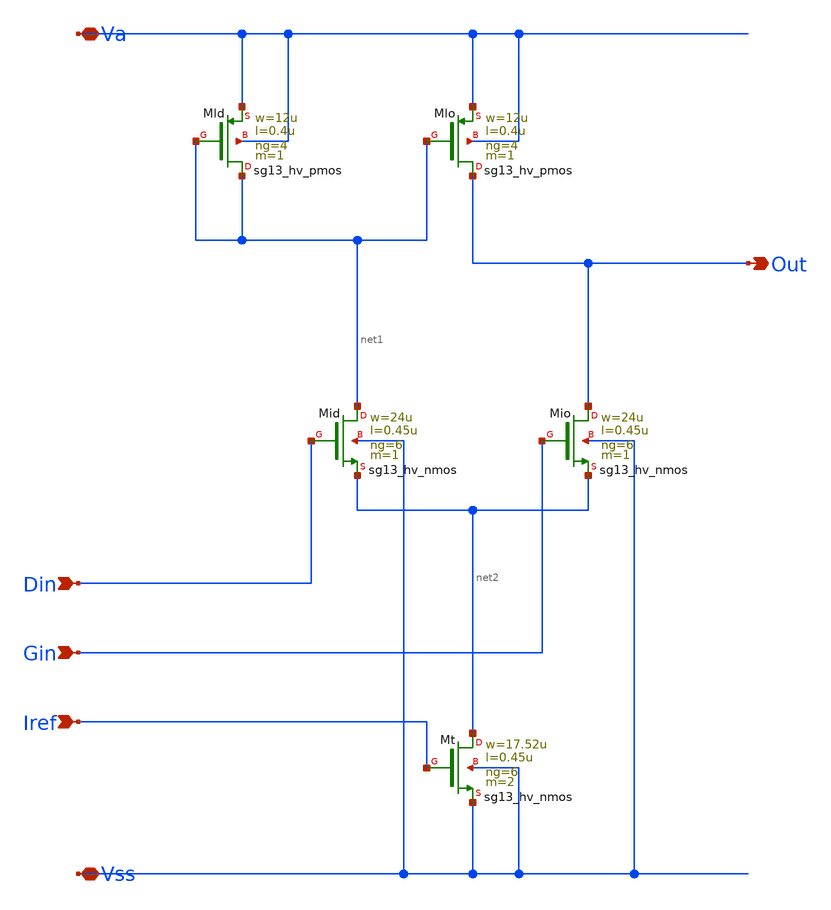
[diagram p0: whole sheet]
** sch_path: macros/lvds_tx/schematic/xschem/predriver_comp.sch
**.subckt predriver_comp Va Vss Out Din Gin Iref
*.iopin Va
*.iopin Vss
*.opin Out
*.ipin Din
*.ipin Gin
*.ipin Iref
XMld net1 net1 Va Va sg13_hv_pmos w=12u l=0.4u ng=4 m=1 mm_ok=1
XMlo Out net1 Va Va sg13_hv_pmos w=12u l=0.4u ng=4 m=1 mm_ok=1
XMid net1 Din net2 Vss sg13_hv_nmos w=24u l=0.45u ng=6 m=1 mm_ok=1
XMio Out Gin net2 Vss sg13_hv_nmos w=24u l=0.45u ng=6 m=1 mm_ok=1
XMt net2 Iref Vss Vss sg13_hv_nmos w=17.52u l=0.45u ng=6 m=2 mm_ok=1
**.ends
.end
